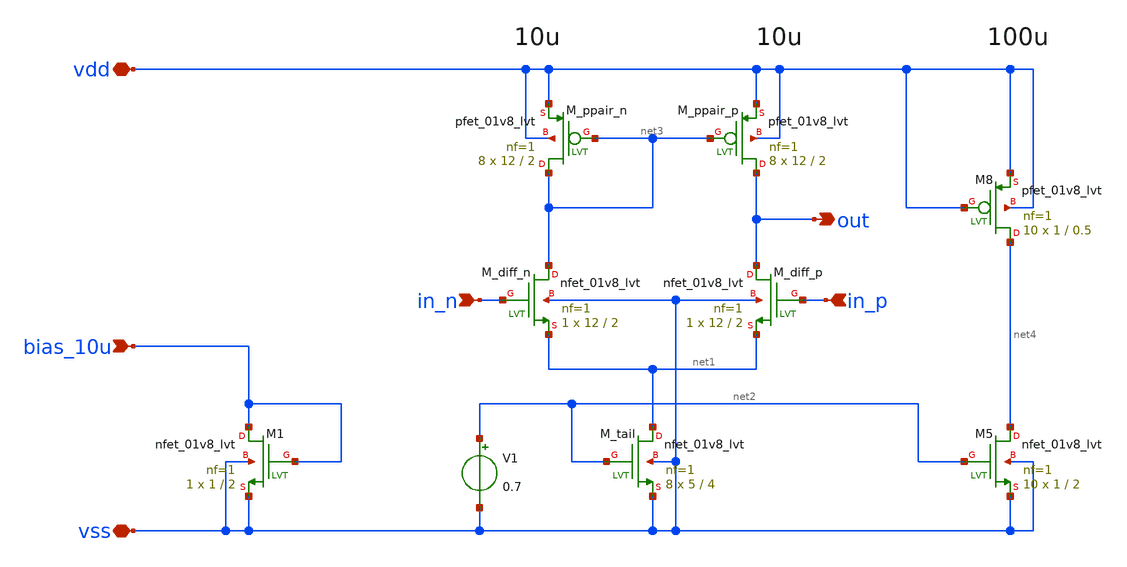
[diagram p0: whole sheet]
** sch_path: design/opamp/5T.sch
**.subckt 5T vdd vss in_n in_p out bias_10u
*.iopin vdd
*.iopin vss
*.ipin in_n
*.ipin in_p
*.opin out
*.ipin bias_10u
XM1 bias_10u bias_10u vss vss sky130_fd_pr__nfet_01v8_lvt L=2 W=1 nf=1 ad='int((nf+1)/2) * W/nf * 0.29'
+ as='int((nf+2)/2) * W/nf * 0.29' pd='2*int((nf+1)/2) * (W/nf + 0.29)' ps='2*int((nf+2)/2) * (W/nf + 0.29)'
+ nrd='0.29 / W' nrs='0.29 / W' sa=0 sb=0 sd=0 mult=1 m=1
XM_diff_n net3 in_n net1 vss sky130_fd_pr__nfet_01v8_lvt L=2 W=12 nf=1 ad='int((nf+1)/2) * W/nf * 0.29'
+ as='int((nf+2)/2) * W/nf * 0.29' pd='2*int((nf+1)/2) * (W/nf + 0.29)' ps='2*int((nf+2)/2) * (W/nf + 0.29)'
+ nrd='0.29 / W' nrs='0.29 / W' sa=0 sb=0 sd=0 mult=1 m=1
XM_diff_p out in_p net1 vss sky130_fd_pr__nfet_01v8_lvt L=2 W=12 nf=1 ad='int((nf+1)/2) * W/nf * 0.29'
+ as='int((nf+2)/2) * W/nf * 0.29' pd='2*int((nf+1)/2) * (W/nf + 0.29)' ps='2*int((nf+2)/2) * (W/nf + 0.29)'
+ nrd='0.29 / W' nrs='0.29 / W' sa=0 sb=0 sd=0 mult=1 m=1
XM_tail net1 net2 vss vss sky130_fd_pr__nfet_01v8_lvt L=4 W=5 nf=1 ad='int((nf+1)/2) * W/nf * 0.29' as='int((nf+2)/2) * W/nf * 0.29'
+ pd='2*int((nf+1)/2) * (W/nf + 0.29)' ps='2*int((nf+2)/2) * (W/nf + 0.29)' nrd='0.29 / W' nrs='0.29 / W'
+ sa=0 sb=0 sd=0 mult=8 m=8
XM5 net4 net2 vss vss sky130_fd_pr__nfet_01v8_lvt L=2 W=1 nf=1 ad='int((nf+1)/2) * W/nf * 0.29' as='int((nf+2)/2) * W/nf * 0.29'
+ pd='2*int((nf+1)/2) * (W/nf + 0.29)' ps='2*int((nf+2)/2) * (W/nf + 0.29)' nrd='0.29 / W' nrs='0.29 / W'
+ sa=0 sb=0 sd=0 mult=10 m=10
XM_ppair_p out net3 vdd vdd sky130_fd_pr__pfet_01v8_lvt L=2 W=12 nf=1 ad='int((nf+1)/2) * W/nf * 0.29'
+ as='int((nf+2)/2) * W/nf * 0.29' pd='2*int((nf+1)/2) * (W/nf + 0.29)' ps='2*int((nf+2)/2) * (W/nf + 0.29)'
+ nrd='0.29 / W' nrs='0.29 / W' sa=0 sb=0 sd=0 mult=8 m=8
XM_ppair_n net3 net3 vdd vdd sky130_fd_pr__pfet_01v8_lvt L=2 W=12 nf=1 ad='int((nf+1)/2) * W/nf * 0.29'
+ as='int((nf+2)/2) * W/nf * 0.29' pd='2*int((nf+1)/2) * (W/nf + 0.29)' ps='2*int((nf+2)/2) * (W/nf + 0.29)'
+ nrd='0.29 / W' nrs='0.29 / W' sa=0 sb=0 sd=0 mult=8 m=8
XM8 net4 vdd vdd vdd sky130_fd_pr__pfet_01v8_lvt L=0.5 W=1 nf=1 ad='int((nf+1)/2) * W/nf * 0.29' as='int((nf+2)/2) * W/nf * 0.29'
+ pd='2*int((nf+1)/2) * (W/nf + 0.29)' ps='2*int((nf+2)/2) * (W/nf + 0.29)' nrd='0.29 / W' nrs='0.29 / W'
+ sa=0 sb=0 sd=0 mult=10 m=10
V1 net2 vss 0.7
**.ends
.end
